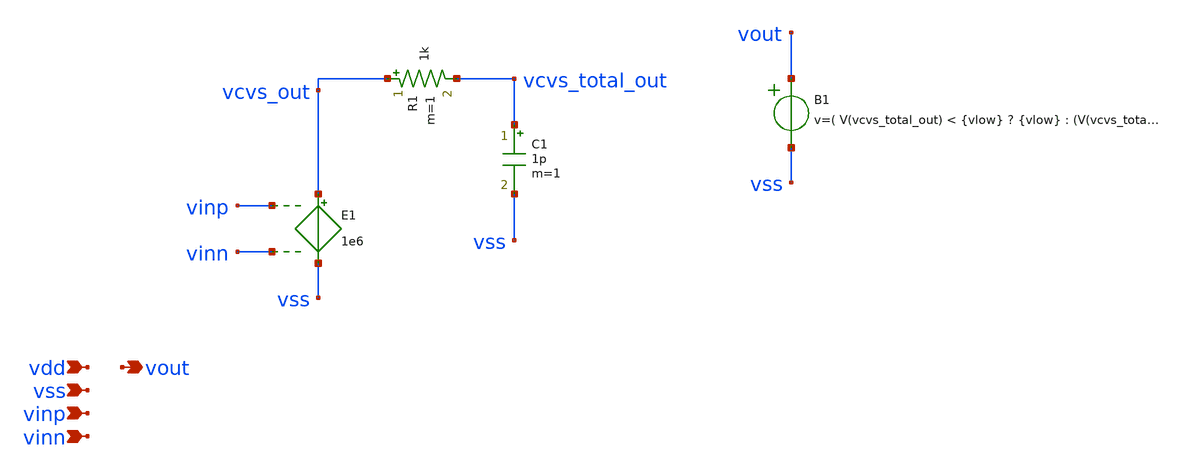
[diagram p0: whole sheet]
** sch_path: schematics/ideal_comp.sch
**.subckt ideal_comp vdd vout vss vinp vinn
*.ipin vdd
*.opin vout
*.ipin vss
*.ipin vinp
*.ipin vinn
E1 vcvs_out vss vinp vinn 1e6
B1 vout vss v=( V(vcvs_total_out) < {vlow} ? {vlow} : (V(vcvs_total_out) > {vhigh} ? {vhigh} : V(vcvs_out)))
R1 vcvs_out vcvs_total_out 1k m=1
C1 vcvs_total_out vss 1p m=1
**.ends
.end
